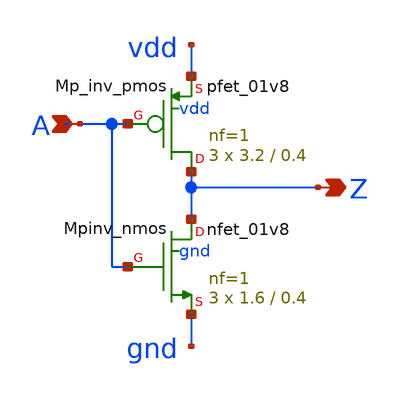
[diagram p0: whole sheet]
** sch_path: sram_2_64_scn4m/pinv_7.sch
**.subckt pinv_7 A Z
*.ipin A
*.opin Z
XMpinv_nmos Z A gnd gnd sky130_fd_pr__nfet_01v8 L=0.4 W=1.6 nf=1 ad='int((nf+1)/2) * W/nf * 0.29' as='int((nf+2)/2) * W/nf * 0.29'
+ pd='2*int((nf+1)/2) * (W/nf + 0.29)' ps='2*int((nf+2)/2) * (W/nf + 0.29)' nrd='0.29 / W' nrs='0.29 / W'
+ sa=0 sb=0 sd=0 mult=3 m=3
XMp_inv_pmos Z A vdd vdd sky130_fd_pr__pfet_01v8 L=0.4 W=3.2 nf=1 ad='int((nf+1)/2) * W/nf * 0.29' as='int((nf+2)/2) * W/nf * 0.29'
+ pd='2*int((nf+1)/2) * (W/nf + 0.29)' ps='2*int((nf+2)/2) * (W/nf + 0.29)' nrd='0.29 / W' nrs='0.29 / W'
+ sa=0 sb=0 sd=0 mult=3 m=3
**.ends
.end
